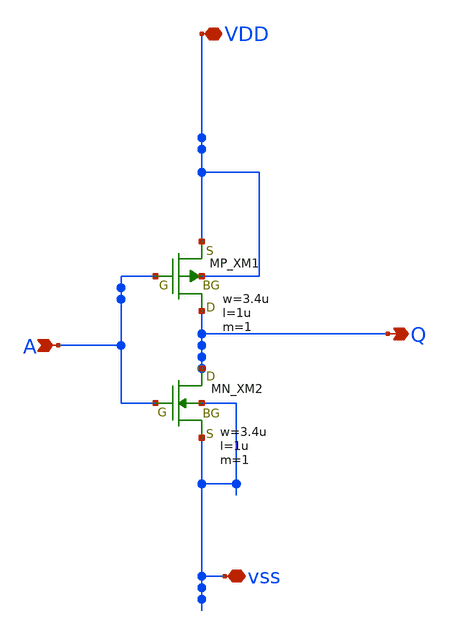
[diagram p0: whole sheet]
** sch_path: inverter/inverter_Tanaka_Airi.sch
**.subckt inverter_Tanaka_Airi A VDD Q vss
*.ipin A
*.iopin VDD
*.opin Q
*.iopin vss
XXM1 Q A VDD VDD PMOS w=3.4u l=1u nrd=0 nrs=0 m=1
XXM2 Q A vss vss NMOS w=3.4u l=1u nrd=0 nrs=0 m=1
**.ends
.end
